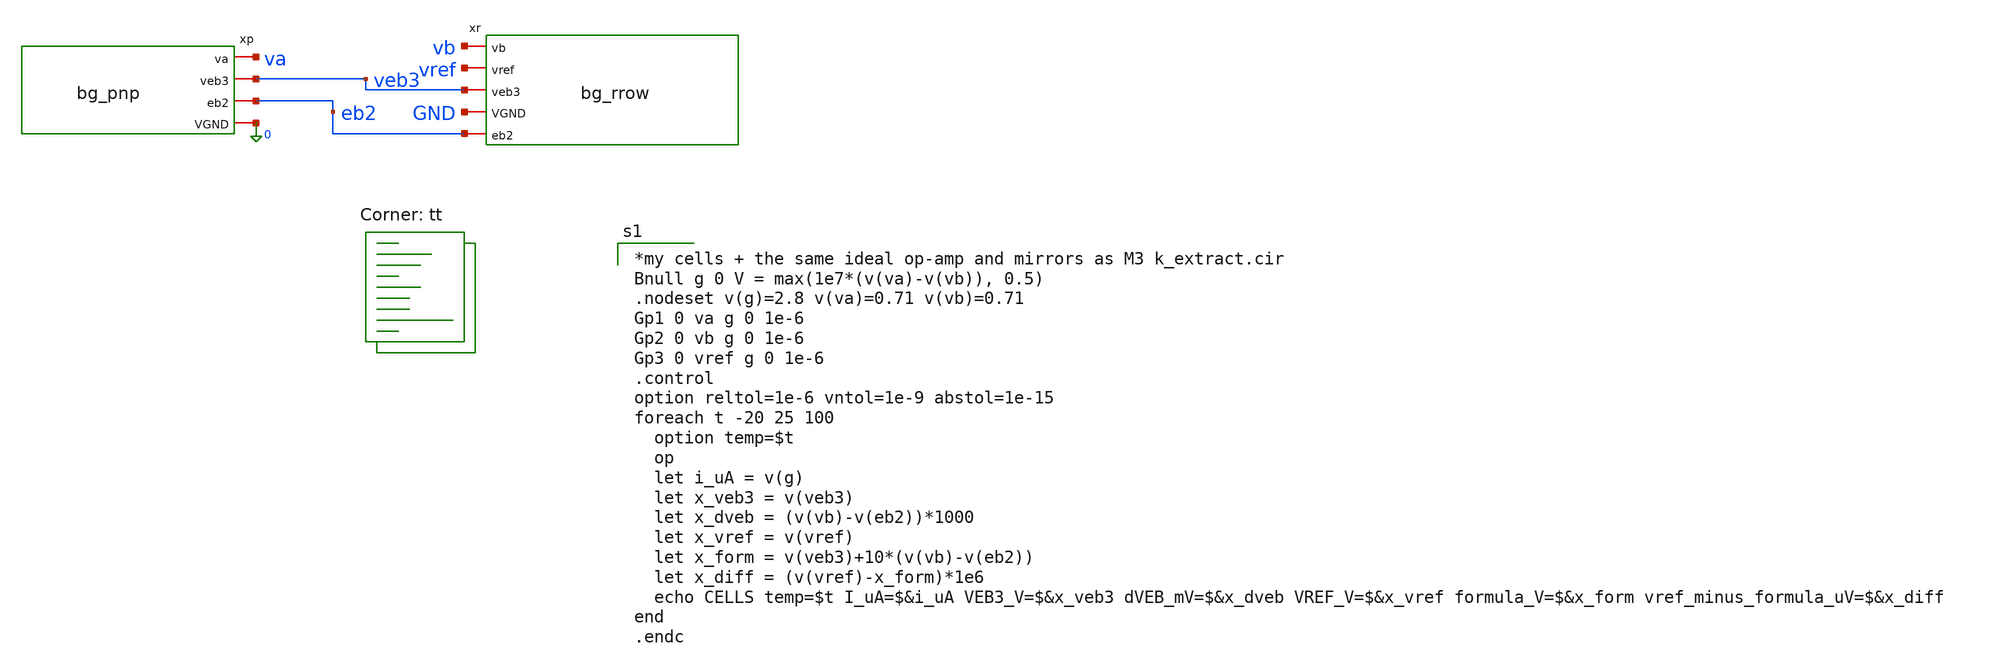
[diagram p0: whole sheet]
** sch_path: xschem/tb_bg_cells.sch
**.subckt tb_bg_cells
xp va veb3 eb2 0 bg_pnp
xr vb vref veb3 GND eb2 bg_rrow
**** begin user architecture code

*my cells + the same ideal op-amp and mirrors as M3 k_extract.cir
Bnull g 0 V = max(1e7*(v(va)-v(vb)), 0.5)
.nodeset v(g)=2.8 v(va)=0.71 v(vb)=0.71
Gp1 0 va g 0 1e-6
Gp2 0 vb g 0 1e-6
Gp3 0 vref g 0 1e-6
.control
option reltol=1e-6 vntol=1e-9 abstol=1e-15
foreach t -20 25 100
  option temp=$t
  op
  let i_uA = v(g)
  let x_veb3 = v(veb3)
  let x_dveb = (v(vb)-v(eb2))*1000
  let x_vref = v(vref)
  let x_form = v(veb3)+10*(v(vb)-v(eb2))
  let x_diff = (v(vref)-x_form)*1e6
  echo CELLS temp=$t I_uA=$&i_uA VEB3_V=$&x_veb3 dVEB_mV=$&x_dveb VREF_V=$&x_vref formula_V=$&x_form
+ vref_minus_formula_uV=$&x_diff
end
.endc

.lib $::SKYWATER_MODELS/sky130.lib.spice tt
**** end user architecture code
**.ends

* expanding   symbol:  bg_pnp.sym # of pins=4
** sym_path: xschem/bg_pnp.sym
** sch_path: xschem/bg_pnp.sch
.subckt bg_pnp va veb3 eb2 VGND
*.iopin va
*.iopin eb2
*.iopin veb3
*.iopin VGND
XQ1 VGND VGND va sky130_fd_pr__pnp_05v5_W3p40L3p40 m=1
XQ2 VGND VGND eb2 sky130_fd_pr__pnp_05v5_W3p40L3p40 m=8
XQ3 VGND VGND veb3 sky130_fd_pr__pnp_05v5_W3p40L3p40 m=1
XQD VGND VGND VGND sky130_fd_pr__pnp_05v5_W3p40L3p40 m=15
.ends


* expanding   symbol:  bg_rrow.sym # of pins=5
** sym_path: xschem/bg_rrow.sym
** sch_path: xschem/bg_rrow.sch
.subckt bg_rrow vb vref veb3 VGND eb2
*.iopin vb
*.iopin eb2
*.iopin vref
*.iopin veb3
*.iopin VGND
XR1_1 eb2 net1 VGND sky130_fd_pr__res_high_po_1p41 L=20 mult=1 m=1
XR1_2 net1 net2 VGND sky130_fd_pr__res_high_po_1p41 L=20 mult=1 m=1
XR1_3 net2 net3 VGND sky130_fd_pr__res_high_po_1p41 L=20 mult=1 m=1
XR1_4 net3 vb VGND sky130_fd_pr__res_high_po_1p41 L=20 mult=1 m=1
XR3[39] r3n[38] vref VGND sky130_fd_pr__res_high_po_1p41 L=20 mult=1 m=1
XR3[38] r3n[37] r3n[38] VGND sky130_fd_pr__res_high_po_1p41 L=20 mult=1 m=1
XR3[37] r3n[36] r3n[37] VGND sky130_fd_pr__res_high_po_1p41 L=20 mult=1 m=1
XR3[36] r3n[35] r3n[36] VGND sky130_fd_pr__res_high_po_1p41 L=20 mult=1 m=1
XR3[35] r3n[34] r3n[35] VGND sky130_fd_pr__res_high_po_1p41 L=20 mult=1 m=1
XR3[34] r3n[33] r3n[34] VGND sky130_fd_pr__res_high_po_1p41 L=20 mult=1 m=1
XR3[33] r3n[32] r3n[33] VGND sky130_fd_pr__res_high_po_1p41 L=20 mult=1 m=1
XR3[32] r3n[31] r3n[32] VGND sky130_fd_pr__res_high_po_1p41 L=20 mult=1 m=1
XR3[31] r3n[30] r3n[31] VGND sky130_fd_pr__res_high_po_1p41 L=20 mult=1 m=1
XR3[30] r3n[29] r3n[30] VGND sky130_fd_pr__res_high_po_1p41 L=20 mult=1 m=1
XR3[29] r3n[28] r3n[29] VGND sky130_fd_pr__res_high_po_1p41 L=20 mult=1 m=1
XR3[28] r3n[27] r3n[28] VGND sky130_fd_pr__res_high_po_1p41 L=20 mult=1 m=1
XR3[27] r3n[26] r3n[27] VGND sky130_fd_pr__res_high_po_1p41 L=20 mult=1 m=1
XR3[26] r3n[25] r3n[26] VGND sky130_fd_pr__res_high_po_1p41 L=20 mult=1 m=1
XR3[25] r3n[24] r3n[25] VGND sky130_fd_pr__res_high_po_1p41 L=20 mult=1 m=1
XR3[24] r3n[23] r3n[24] VGND sky130_fd_pr__res_high_po_1p41 L=20 mult=1 m=1
XR3[23] r3n[22] r3n[23] VGND sky130_fd_pr__res_high_po_1p41 L=20 mult=1 m=1
XR3[22] r3n[21] r3n[22] VGND sky130_fd_pr__res_high_po_1p41 L=20 mult=1 m=1
XR3[21] r3n[20] r3n[21] VGND sky130_fd_pr__res_high_po_1p41 L=20 mult=1 m=1
XR3[20] r3n[19] r3n[20] VGND sky130_fd_pr__res_high_po_1p41 L=20 mult=1 m=1
XR3[19] r3n[18] r3n[19] VGND sky130_fd_pr__res_high_po_1p41 L=20 mult=1 m=1
XR3[18] r3n[17] r3n[18] VGND sky130_fd_pr__res_high_po_1p41 L=20 mult=1 m=1
XR3[17] r3n[16] r3n[17] VGND sky130_fd_pr__res_high_po_1p41 L=20 mult=1 m=1
XR3[16] r3n[15] r3n[16] VGND sky130_fd_pr__res_high_po_1p41 L=20 mult=1 m=1
XR3[15] r3n[14] r3n[15] VGND sky130_fd_pr__res_high_po_1p41 L=20 mult=1 m=1
XR3[14] r3n[13] r3n[14] VGND sky130_fd_pr__res_high_po_1p41 L=20 mult=1 m=1
XR3[13] r3n[12] r3n[13] VGND sky130_fd_pr__res_high_po_1p41 L=20 mult=1 m=1
XR3[12] r3n[11] r3n[12] VGND sky130_fd_pr__res_high_po_1p41 L=20 mult=1 m=1
XR3[11] r3n[10] r3n[11] VGND sky130_fd_pr__res_high_po_1p41 L=20 mult=1 m=1
XR3[10] r3n[9] r3n[10] VGND sky130_fd_pr__res_high_po_1p41 L=20 mult=1 m=1
XR3[9] r3n[8] r3n[9] VGND sky130_fd_pr__res_high_po_1p41 L=20 mult=1 m=1
XR3[8] r3n[7] r3n[8] VGND sky130_fd_pr__res_high_po_1p41 L=20 mult=1 m=1
XR3[7] r3n[6] r3n[7] VGND sky130_fd_pr__res_high_po_1p41 L=20 mult=1 m=1
XR3[6] r3n[5] r3n[6] VGND sky130_fd_pr__res_high_po_1p41 L=20 mult=1 m=1
XR3[5] r3n[4] r3n[5] VGND sky130_fd_pr__res_high_po_1p41 L=20 mult=1 m=1
XR3[4] r3n[3] r3n[4] VGND sky130_fd_pr__res_high_po_1p41 L=20 mult=1 m=1
XR3[3] r3n[2] r3n[3] VGND sky130_fd_pr__res_high_po_1p41 L=20 mult=1 m=1
XR3[2] r3n[1] r3n[2] VGND sky130_fd_pr__res_high_po_1p41 L=20 mult=1 m=1
XR3[1] r3n[0] r3n[1] VGND sky130_fd_pr__res_high_po_1p41 L=20 mult=1 m=1
XR3[0] veb3 r3n[0] VGND sky130_fd_pr__res_high_po_1p41 L=20 mult=1 m=1
XRD[3] VGND VGND VGND sky130_fd_pr__res_high_po_1p41 L=20 mult=1 m=1
XRD[2] VGND VGND VGND sky130_fd_pr__res_high_po_1p41 L=20 mult=1 m=1
XRD[1] VGND VGND VGND sky130_fd_pr__res_high_po_1p41 L=20 mult=1 m=1
XRD[0] VGND VGND VGND sky130_fd_pr__res_high_po_1p41 L=20 mult=1 m=1
.ends

.end
